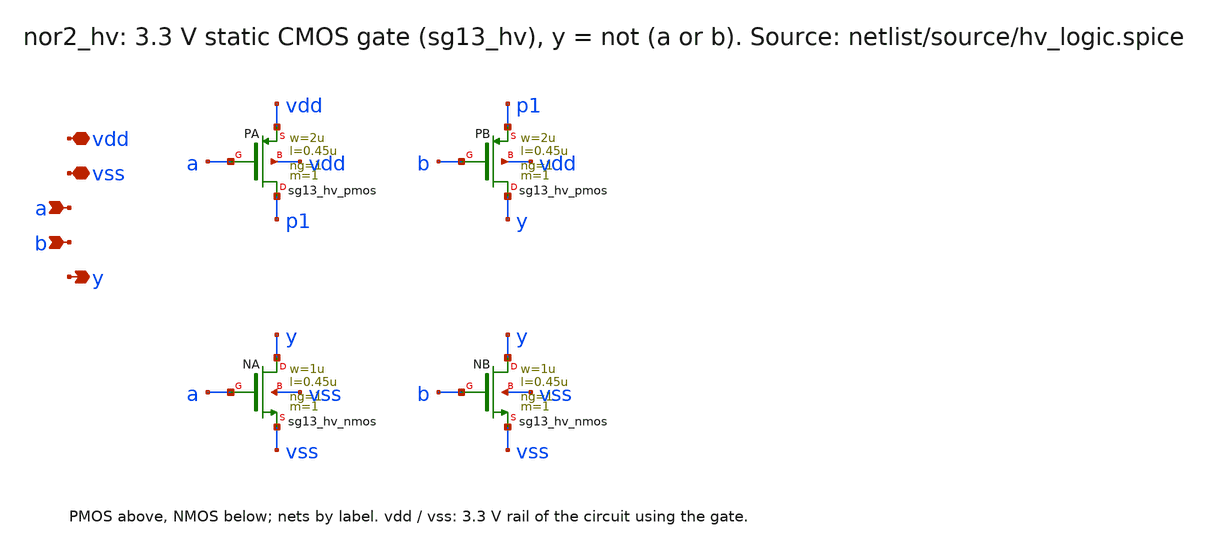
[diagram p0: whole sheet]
** sch_path: sudelbuecher/design_considerations/consolidation/bias_hierarchy_2026-10-27/before/macros/hv_logic/schematic/xschem/nor2_hv.sch
**.subckt nor2_hv vdd vss a b y
*.iopin vdd
*.iopin vss
*.ipin a
*.ipin b
*.opin y
XPA p1 a vdd vdd sg13_hv_pmos w=2u l=0.45u ng=1 m=1 mm_ok=1
XPB y b p1 vdd sg13_hv_pmos w=2u l=0.45u ng=1 m=1 mm_ok=1
XNA y a vss vss sg13_hv_nmos w=1u l=0.45u ng=1 m=1 mm_ok=1
XNB y b vss vss sg13_hv_nmos w=1u l=0.45u ng=1 m=1 mm_ok=1
**.ends
.end
